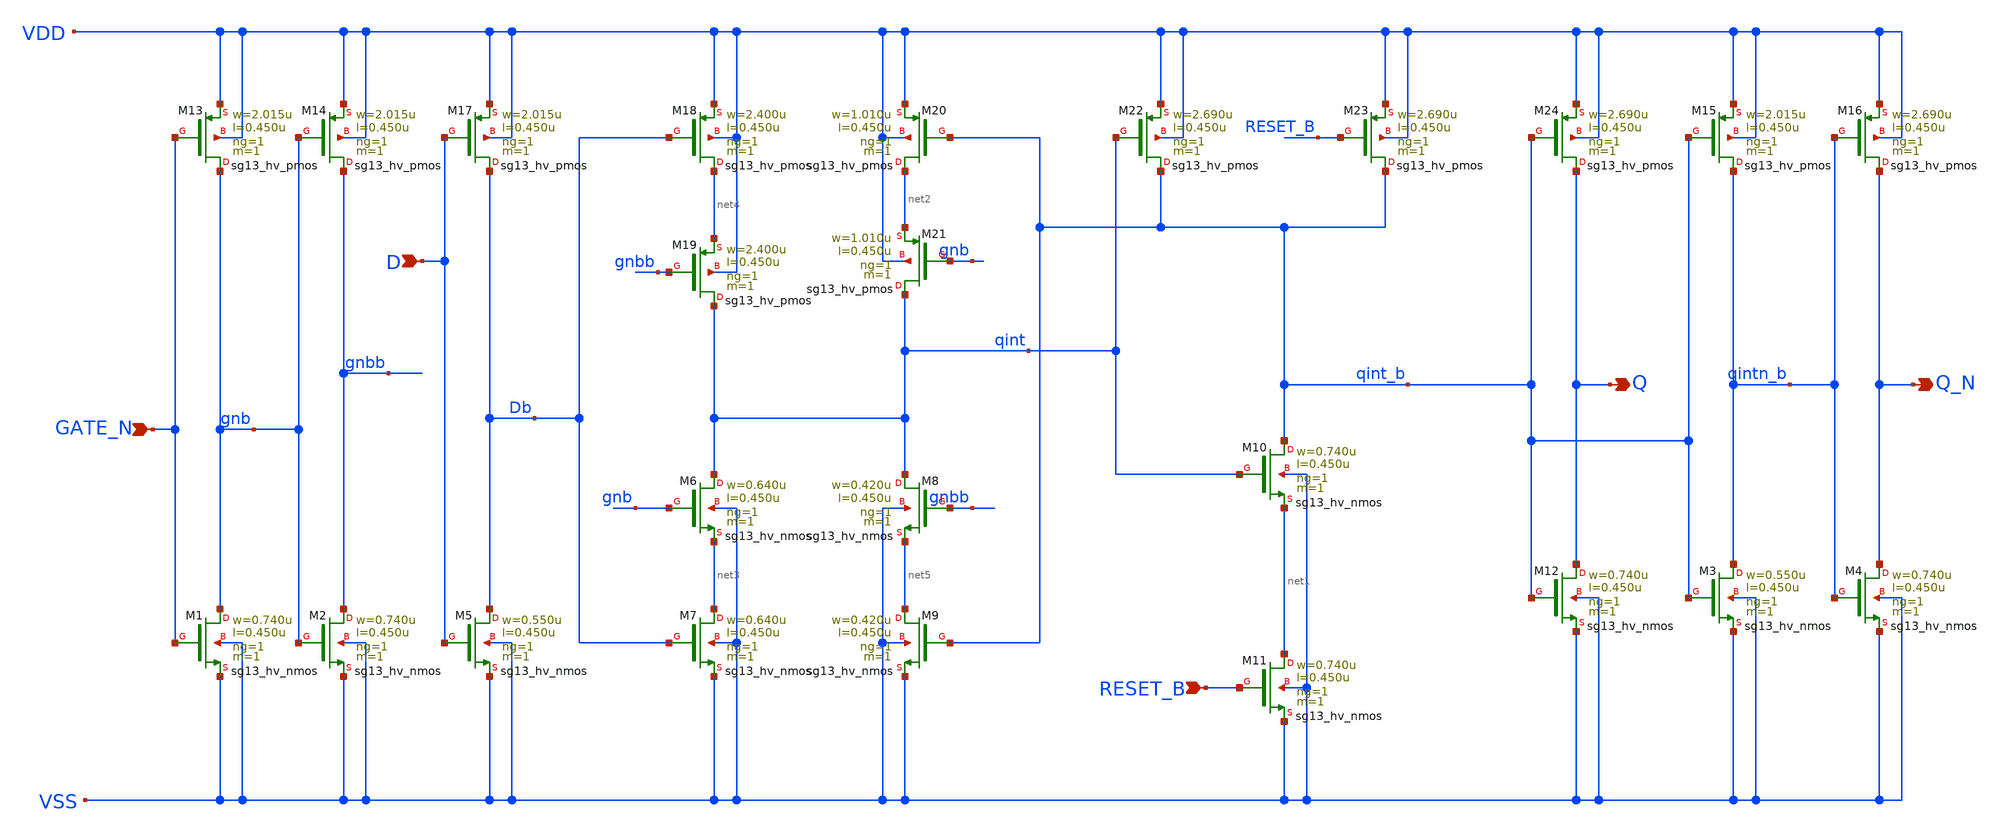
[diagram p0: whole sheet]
** sch_path: ihp-sg13g2/libs.ref/sg13g2_stdcell_hv/sch/xschem/sg13g2_hv_dllr_1.sch
* Copyright 2023 IHP PDK Authors
* Licensed under the Apache License, Version 2.0 (the "License");
* you may not use this file except in compliance with the License.
* You may obtain a copy of the License at
* https://www.apache.org/licenses/LICENSE-2.0
* Unless required by applicable law or agreed to in writing, software
* distributed under the License is distributed on an "AS IS" BASIS,
* WITHOUT WARRANTIES OR CONDITIONS OF ANY KIND, either express or implied.
* See the License for the specific language governing permissions and
* limitations under the License.
**.subckt sg13g2_hv_dllr_1 D GATE_N RESET_B Q Q_N
*.ipin D
*.ipin GATE_N
*.ipin RESET_B
*.opin Q
*.opin Q_N
XM1 gnb GATE_N VSS VSS sg13_hv_nmos w=0.740u l=0.450u ng=1 m=1 mm_ok=1
XM2 gnbb gnb VSS VSS sg13_hv_nmos w=0.740u l=0.450u ng=1 m=1 mm_ok=1
XM3 qintn_b qint_b VSS VSS sg13_hv_nmos w=0.550u l=0.450u ng=1 m=1 mm_ok=1
XM4 Q_N qintn_b VSS VSS sg13_hv_nmos w=0.740u l=0.450u ng=1 m=1 mm_ok=1
XM5 Db D VSS VSS sg13_hv_nmos w=0.550u l=0.450u ng=1 m=1 mm_ok=1
XM6 qint gnb net3 VSS sg13_hv_nmos w=0.640u l=0.450u ng=1 m=1 mm_ok=1
XM7 net3 Db VSS VSS sg13_hv_nmos w=0.640u l=0.450u ng=1 m=1 mm_ok=1
XM8 qint gnbb net5 VSS sg13_hv_nmos w=0.420u l=0.450u ng=1 m=1 mm_ok=1
XM9 net5 qint_b VSS VSS sg13_hv_nmos w=0.420u l=0.450u ng=1 m=1 mm_ok=1
XM10 qint_b qint net1 VSS sg13_hv_nmos w=0.740u l=0.450u ng=1 m=1 mm_ok=1
XM11 net1 RESET_B VSS VSS sg13_hv_nmos w=0.740u l=0.450u ng=1 m=1 mm_ok=1
XM12 Q qint_b VSS VSS sg13_hv_nmos w=0.740u l=0.450u ng=1 m=1 mm_ok=1
XM13 gnb GATE_N VDD VDD sg13_hv_pmos w=2.015u l=0.450u ng=1 m=1 mm_ok=1
XM14 gnbb gnb VDD VDD sg13_hv_pmos w=2.015u l=0.450u ng=1 m=1 mm_ok=1
XM15 qintn_b qint_b VDD VDD sg13_hv_pmos w=2.015u l=0.450u ng=1 m=1 mm_ok=1
XM16 Q_N qintn_b VDD VDD sg13_hv_pmos w=2.690u l=0.450u ng=1 m=1 mm_ok=1
XM17 Db D VDD VDD sg13_hv_pmos w=2.015u l=0.450u ng=1 m=1 mm_ok=1
XM18 net4 Db VDD VDD sg13_hv_pmos w=2.400u l=0.450u ng=1 m=1 mm_ok=1
XM19 qint gnbb net4 VDD sg13_hv_pmos w=2.400u l=0.450u ng=1 m=1 mm_ok=1
XM20 net2 qint_b VDD VDD sg13_hv_pmos w=1.010u l=0.450u ng=1 m=1 mm_ok=1
XM21 qint gnb net2 VDD sg13_hv_pmos w=1.010u l=0.450u ng=1 m=1 mm_ok=1
XM22 qint_b qint VDD VDD sg13_hv_pmos w=2.690u l=0.450u ng=1 m=1 mm_ok=1
XM23 qint_b RESET_B VDD VDD sg13_hv_pmos w=2.690u l=0.450u ng=1 m=1 mm_ok=1
XM24 Q qint_b VDD VDD sg13_hv_pmos w=2.690u l=0.450u ng=1 m=1 mm_ok=1
**.ends
.end
